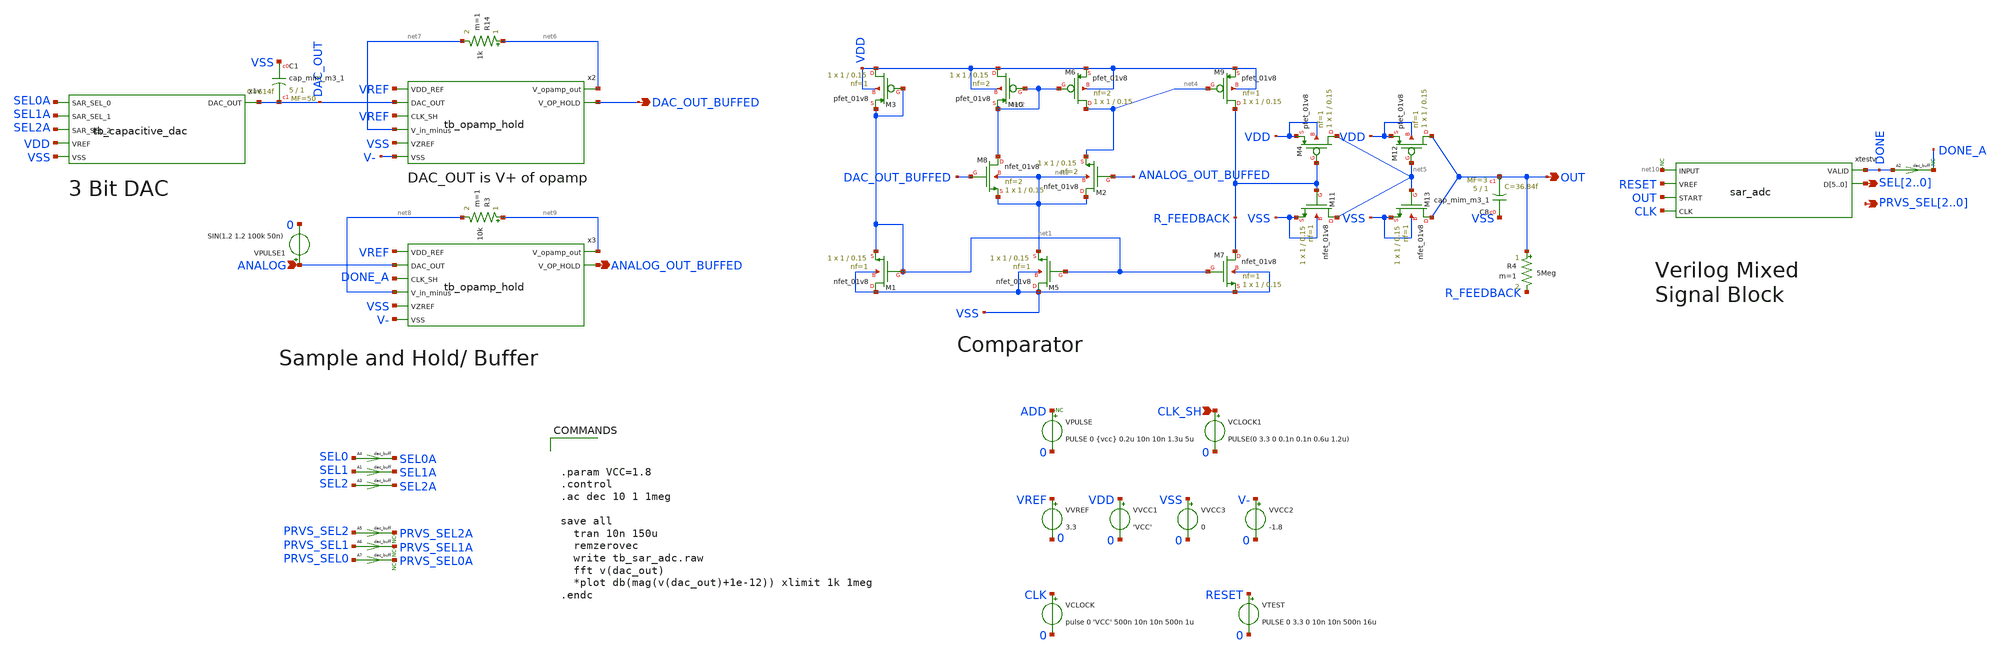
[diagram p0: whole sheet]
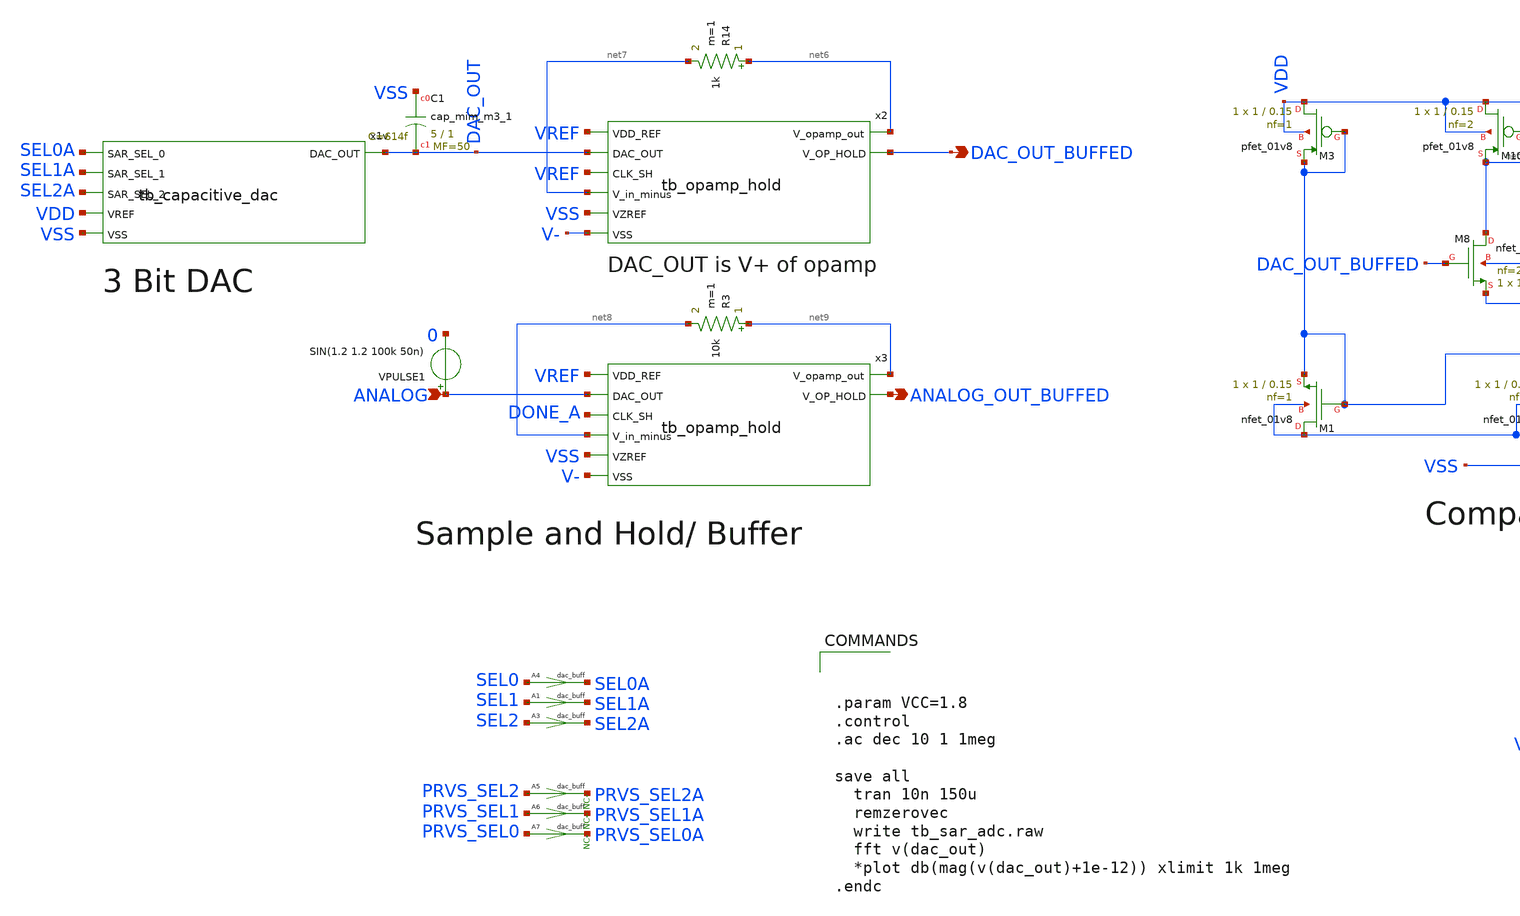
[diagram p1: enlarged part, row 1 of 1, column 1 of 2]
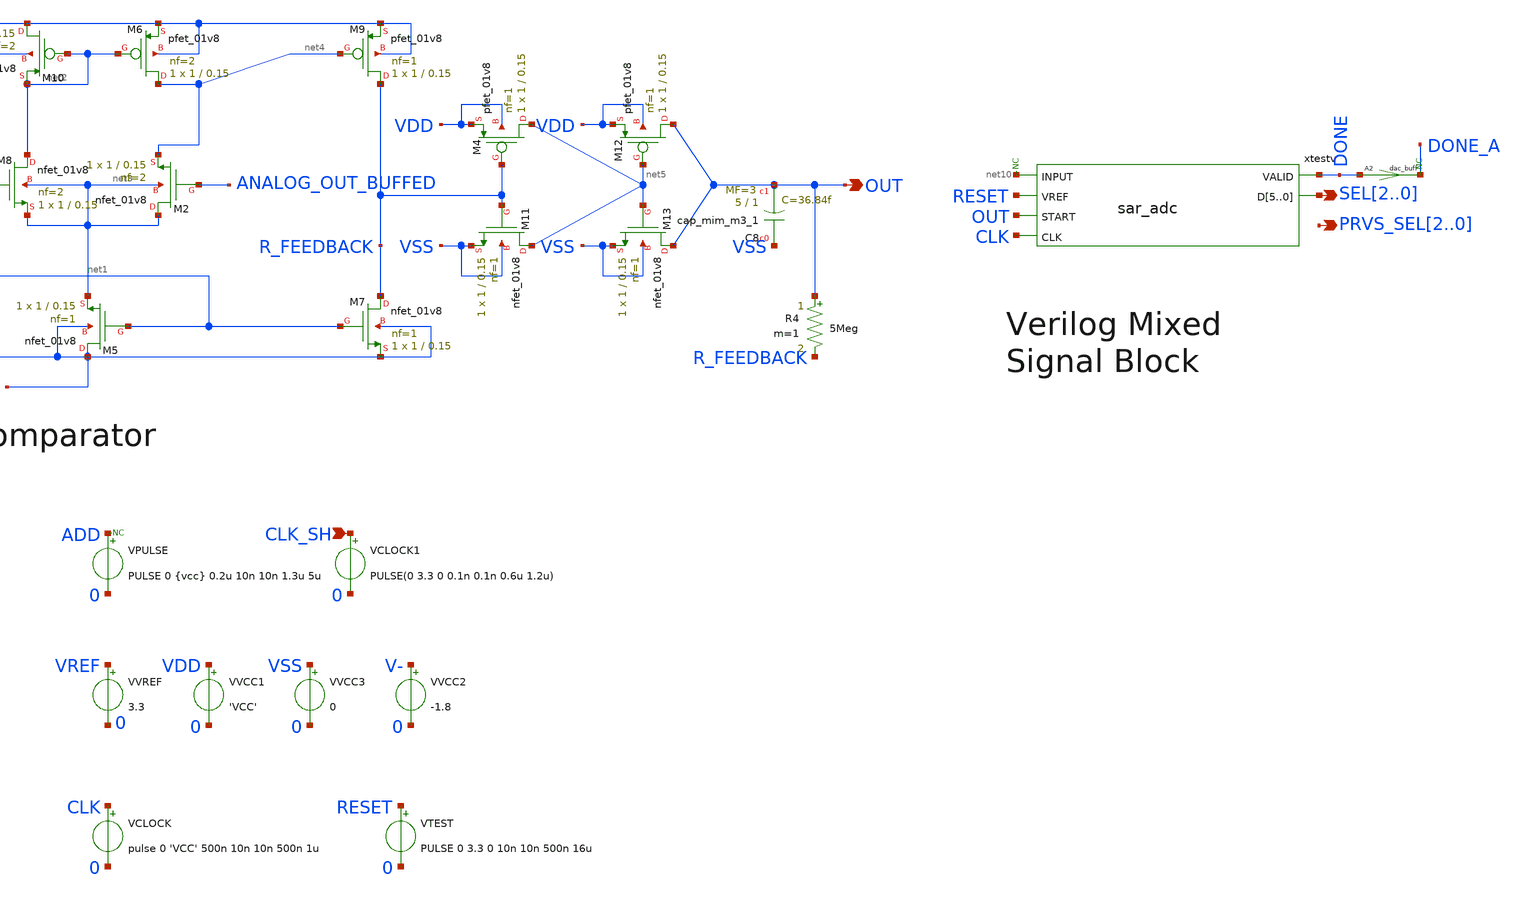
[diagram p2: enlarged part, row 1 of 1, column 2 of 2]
** sch_path: 3bit_sar_adc/tb_sar_adc.sch
**.subckt tb_sar_adc SEL2,SEL1,SEL0 PRVS_SEL2,PRVS_SEL1,PRVS_SEL0 OUT ANALOG DAC_OUT_BUFFED
*+ ANALOG_OUT_BUFFED CLK_SH
*.opin SEL2,SEL1,SEL0
*.opin PRVS_SEL2,PRVS_SEL1,PRVS_SEL0
*.opin OUT
*.ipin ANALOG
*.opin DAC_OUT_BUFFED
*.opin ANALOG_OUT_BUFFED
*.ipin CLK_SH
VPULSE ADD 0 PULSE 0 {vcc} 0.2u 10n 10n 1.3u 5u
VTEST RESET 0 PULSE 0 3.3 0 10n 10n 500n 16u
xtestv net10 RESET OUT DONE SEL2 SEL1 SEL0 SEL2 SEL1 SEL0 CLK sar_adc
A2 [ DONE ] [ DONE_A ] dac_buff
VCLOCK CLK 0 pulse 0 'VCC' 500n 10n 10n 500n 1u
A1 [ SEL1 ] [ SEL1A ] dac_buff
A3 [ SEL2 ] [ SEL2A ] dac_buff
A4 [ SEL0 ] [ SEL0A ] dac_buff
A5 [ PRVS_SEL2 ] [ PRVS_SEL2A ] dac_buff
A6 [ PRVS_SEL1 ] [ PRVS_SEL1A ] dac_buff
A7 [ PRVS_SEL0 ] [ PRVS_SEL0A ] dac_buff
XM9 R_FEEDBACK net4 VDD VDD sky130_fd_pr__pfet_01v8 L=0.15 W=1 nf=1 ad='int((nf+1)/2) * W/nf * 0.29'
+ as='int((nf+2)/2) * W/nf * 0.29' pd='2*int((nf+1)/2) * (W/nf + 0.29)' ps='2*int((nf+2)/2) * (W/nf + 0.29)'
+ nrd='0.29 / W' nrs='0.29 / W' sa=0 sb=0 sd=0 mult=1 m=1
XM6 net4 net2 VDD VDD sky130_fd_pr__pfet_01v8 L=0.15 W=1 nf=2 ad='int((nf+1)/2) * W/nf * 0.29' as='int((nf+2)/2) * W/nf * 0.29'
+ pd='2*int((nf+1)/2) * (W/nf + 0.29)' ps='2*int((nf+2)/2) * (W/nf + 0.29)' nrd='0.29 / W' nrs='0.29 / W'
+ sa=0 sb=0 sd=0 mult=1 m=1
XM10 VDD net2 net2 VDD sky130_fd_pr__pfet_01v8 L=0.15 W=1 nf=2 ad='int((nf+1)/2) * W/nf * 0.29' as='int((nf+2)/2) * W/nf * 0.29'
+ pd='2*int((nf+1)/2) * (W/nf + 0.29)' ps='2*int((nf+2)/2) * (W/nf + 0.29)' nrd='0.29 / W' nrs='0.29 / W'
+ sa=0 sb=0 sd=0 mult=1 m=1
XM3 VDD net1 net1 VDD sky130_fd_pr__pfet_01v8 L=0.15 W=1 nf=1 ad='int((nf+1)/2) * W/nf * 0.29' as='int((nf+2)/2) * W/nf * 0.29'
+ pd='2*int((nf+1)/2) * (W/nf + 0.29)' ps='2*int((nf+2)/2) * (W/nf + 0.29)' nrd='0.29 / W' nrs='0.29 / W'
+ sa=0 sb=0 sd=0 mult=1 m=1
XM4 net5 R_FEEDBACK VDD VDD sky130_fd_pr__pfet_01v8 L=0.15 W=1 nf=1 ad='int((nf+1)/2) * W/nf * 0.29'
+ as='int((nf+2)/2) * W/nf * 0.29' pd='2*int((nf+1)/2) * (W/nf + 0.29)' ps='2*int((nf+2)/2) * (W/nf + 0.29)'
+ nrd='0.29 / W' nrs='0.29 / W' sa=0 sb=0 sd=0 mult=1 m=1
XM12 OUT net5 VDD VDD sky130_fd_pr__pfet_01v8 L=0.15 W=1 nf=1 ad='int((nf+1)/2) * W/nf * 0.29' as='int((nf+2)/2) * W/nf * 0.29'
+ pd='2*int((nf+1)/2) * (W/nf + 0.29)' ps='2*int((nf+2)/2) * (W/nf + 0.29)' nrd='0.29 / W' nrs='0.29 / W'
+ sa=0 sb=0 sd=0 mult=1 m=1
XM2 net3 ANALOG_OUT_BUFFED net4 net3 sky130_fd_pr__nfet_01v8 L=0.15 W=1 nf=2 ad='int((nf+1)/2) * W/nf * 0.29'
+ as='int((nf+2)/2) * W/nf * 0.29' pd='2*int((nf+1)/2) * (W/nf + 0.29)' ps='2*int((nf+2)/2) * (W/nf + 0.29)'
+ nrd='0.29 / W' nrs='0.29 / W' sa=0 sb=0 sd=0 mult=1 m=1
XM1 VSS net1 net1 VSS sky130_fd_pr__nfet_01v8 L=0.15 W=1 nf=1 ad='int((nf+1)/2) * W/nf * 0.29' as='int((nf+2)/2) * W/nf * 0.29'
+ pd='2*int((nf+1)/2) * (W/nf + 0.29)' ps='2*int((nf+2)/2) * (W/nf + 0.29)' nrd='0.29 / W' nrs='0.29 / W'
+ sa=0 sb=0 sd=0 mult=1 m=1
XM5 VSS net1 net3 VSS sky130_fd_pr__nfet_01v8 L=0.15 W=1 nf=1 ad='int((nf+1)/2) * W/nf * 0.29' as='int((nf+2)/2) * W/nf * 0.29'
+ pd='2*int((nf+1)/2) * (W/nf + 0.29)' ps='2*int((nf+2)/2) * (W/nf + 0.29)' nrd='0.29 / W' nrs='0.29 / W'
+ sa=0 sb=0 sd=0 mult=1 m=1
XM7 R_FEEDBACK net1 VSS VSS sky130_fd_pr__nfet_01v8 L=0.15 W=1 nf=1 ad='int((nf+1)/2) * W/nf * 0.29'
+ as='int((nf+2)/2) * W/nf * 0.29' pd='2*int((nf+1)/2) * (W/nf + 0.29)' ps='2*int((nf+2)/2) * (W/nf + 0.29)'
+ nrd='0.29 / W' nrs='0.29 / W' sa=0 sb=0 sd=0 mult=1 m=1
XM8 net2 DAC_OUT_BUFFED net3 net3 sky130_fd_pr__nfet_01v8 L=0.15 W=1 nf=2 ad='int((nf+1)/2) * W/nf * 0.29'
+ as='int((nf+2)/2) * W/nf * 0.29' pd='2*int((nf+1)/2) * (W/nf + 0.29)' ps='2*int((nf+2)/2) * (W/nf + 0.29)'
+ nrd='0.29 / W' nrs='0.29 / W' sa=0 sb=0 sd=0 mult=1 m=1
XM11 net5 R_FEEDBACK VSS VSS sky130_fd_pr__nfet_01v8 L=0.15 W=1 nf=1 ad='int((nf+1)/2) * W/nf * 0.29'
+ as='int((nf+2)/2) * W/nf * 0.29' pd='2*int((nf+1)/2) * (W/nf + 0.29)' ps='2*int((nf+2)/2) * (W/nf + 0.29)'
+ nrd='0.29 / W' nrs='0.29 / W' sa=0 sb=0 sd=0 mult=1 m=1
XM13 OUT net5 VSS VSS sky130_fd_pr__nfet_01v8 L=0.15 W=1 nf=1 ad='int((nf+1)/2) * W/nf * 0.29' as='int((nf+2)/2) * W/nf * 0.29'
+ pd='2*int((nf+1)/2) * (W/nf + 0.29)' ps='2*int((nf+2)/2) * (W/nf + 0.29)' nrd='0.29 / W' nrs='0.29 / W'
+ sa=0 sb=0 sd=0 mult=1 m=1
XC8 VSS OUT sky130_fd_pr__cap_mim_m3_1 W=5 L=1 MF=3 m=3
VVCC1 VDD 0 'VCC'
VPULSE1 ANALOG 0 SIN(1.2 1.2 100k 50n)
x1v DAC_OUT SEL0A SEL1A SEL2A VDD VSS tb_capacitive_dac
x2 VREF DAC_OUT VREF net7 net6 DAC_OUT_BUFFED VSS V- tb_opamp_hold
VVREF VREF 0 3.3
x3 VREF ANALOG DONE_A net8 net9 ANALOG_OUT_BUFFED VSS V- tb_opamp_hold
VVCC3 VSS 0 0
VVCC2 V- 0 -1.8
* noconn DONE_A
* noconn ADD
* noconn PRVS_SEL2A
* noconn PRVS_SEL1A
* noconn PRVS_SEL0A
VCLOCK1 CLK_SH 0 PULSE(0 3.3 0 0.1n 0.1n 0.6u 1.2u)
* noconn #net10
XC1 VSS DAC_OUT sky130_fd_pr__cap_mim_m3_1 W=5 L=1 MF=50 m=50
R14 net6 net7 1k m=1
R3 net9 net8 10k m=1
R4 OUT R_FEEDBACK 5Meg m=1
**** begin user architecture code



.param VCC=1.8
.control
.ac dec 10 1 1meg

save all
  tran 10n 150u
  remzerovec
  write tb_sar_adc.raw
  fft v(dac_out)
  *plot db(mag(v(dac_out)+1e-12)) xlimit 1k 1meg
.endc



** opencircuitdesign pdks install
.lib $::SKYWATER_MODELS/sky130.lib.spice tt
.include $::SKYWATER_STDCELLS/sky130_fd_sc_hd.spice
.include /foss/pdks/sky130A/libs.tech/xschem/sky130_stdcells/

**** end user architecture code
**.ends

* expanding   symbol:  /foss/designs/3bit_sar_adc/3bit_sar_adc/sar_adc.sym # of pins=6
** sym_path: /foss/designs/3bit_sar_adc/3bit_sar_adc/sar_adc.sym
** sch_path: /foss/designs/3bit_sar_adc/3bit_sar_adc/sar_adc.sch
.subckt sar_adc INPUT VREF START VALID D5 D4 D3 D2 D1 D0 CLK
*.ipin INPUT
*.ipin VREF
*.ipin START
*.opin VALID
*.ipin CLK
*.opin D5,D4,D3,D2,D1,D0
CLAST TEST_V 0 '1p / 32' m=1
ACOMP [ %vd(TEST_V VREF) ] [ COMP ] comparator
XSAMPLE INPUT IIN SAMPLE VREF tgate
R1 IIN TEST_V 1k m=1
ADUT [ CLK COMP START ] [ SAMPLE ~D5 ~D4 ~D3 VALID VALID VALID ] dut
A1 [ COMP ] [ COMP_A ] dac_buff
* noconn D[5..0]
* noconn COMP
* noconn %vd(TEST_V VREF)
xb6 TEST_V VREF D5 ccap C=1p,'1p/2','1p/4','1p/8','1p/16','1p/32'
xb5 TEST_V VREF D4 ccap C=1p,'1p/2','1p/4','1p/8','1p/16','1p/32'
xb4 TEST_V VREF D3 ccap C=1p,'1p/2','1p/4','1p/8','1p/16','1p/32'
xb3 TEST_V VREF D2 ccap C=1p,'1p/2','1p/4','1p/8','1p/16','1p/32'
xb2 TEST_V VREF D1 ccap C=1p,'1p/2','1p/4','1p/8','1p/16','1p/32'
xb1 TEST_V VREF D0 ccap C=1p,'1p/2','1p/4','1p/8','1p/16','1p/32'
.ends


* expanding   symbol:  /foss/designs/3bit_sar_adc/3bit_sar_adc/tb_capacitive_dac.sym # of pins=6
** sym_path: /foss/designs/3bit_sar_adc/3bit_sar_adc/tb_capacitive_dac.sym
** sch_path: /foss/designs/3bit_sar_adc/3bit_sar_adc/tb_capacitive_dac.sch
.subckt tb_capacitive_dac DAC_OUT SAR_SEL_0 SAR_SEL_1 SAR_SEL_2 VREF VSS
*.opin DAC_OUT
*.ipin SAR_SEL_1
*.ipin SAR_SEL_0
*.ipin SAR_SEL_2
*.ipin VREF
*.ipin VSS
XM20 VSS SAR_SEL_2 S2 S2 sky130_fd_pr__pfet_01v8 L=0.15 W=100 nf=4 ad='int((nf+1)/2) * W/nf * 0.29' as='int((nf+2)/2) * W/nf * 0.29'
+ pd='2*int((nf+1)/2) * (W/nf + 0.29)' ps='2*int((nf+2)/2) * (W/nf + 0.29)' nrd='0.29 / W' nrs='0.29 / W'
+ sa=0 sb=0 sd=0 mult=1 m=1
XM21 VREF SAR_SEL_2 S2 S2 sky130_fd_pr__nfet_01v8 L=0.15 W=150 nf=4 ad='int((nf+1)/2) * W/nf * 0.29'
+ as='int((nf+2)/2) * W/nf * 0.29' pd='2*int((nf+1)/2) * (W/nf + 0.29)' ps='2*int((nf+2)/2) * (W/nf + 0.29)'
+ nrd='0.29 / W' nrs='0.29 / W' sa=0 sb=0 sd=0 mult=1 m=1
XC16 net1 S1 sky130_fd_pr__cap_mim_m3_1 W=5 L=1 MF=400 m=400
XC18 net1 S0 sky130_fd_pr__cap_mim_m3_1 W=5 L=1 MF=200 m=200
XM22 VSS SAR_SEL_1 S1 S1 sky130_fd_pr__pfet_01v8 L=0.15 W=100 nf=10 ad='int((nf+1)/2) * W/nf * 0.29'
+ as='int((nf+2)/2) * W/nf * 0.29' pd='2*int((nf+1)/2) * (W/nf + 0.29)' ps='2*int((nf+2)/2) * (W/nf + 0.29)'
+ nrd='0.29 / W' nrs='0.29 / W' sa=0 sb=0 sd=0 mult=1 m=1
XM23 VREF SAR_SEL_1 S1 S1 sky130_fd_pr__nfet_01v8 L=0.15 W=150 nf=4 ad='int((nf+1)/2) * W/nf * 0.29'
+ as='int((nf+2)/2) * W/nf * 0.29' pd='2*int((nf+1)/2) * (W/nf + 0.29)' ps='2*int((nf+2)/2) * (W/nf + 0.29)'
+ nrd='0.29 / W' nrs='0.29 / W' sa=0 sb=0 sd=0 mult=1 m=1
XM24 VSS SAR_SEL_0 S0 S0 sky130_fd_pr__pfet_01v8 L=0.15 W=100 nf=4 ad='int((nf+1)/2) * W/nf * 0.29' as='int((nf+2)/2) * W/nf * 0.29'
+ pd='2*int((nf+1)/2) * (W/nf + 0.29)' ps='2*int((nf+2)/2) * (W/nf + 0.29)' nrd='0.29 / W' nrs='0.29 / W'
+ sa=0 sb=0 sd=0 mult=1 m=1
XM25 VREF SAR_SEL_0 S0 S0 sky130_fd_pr__nfet_01v8 L=0.15 W=150 nf=4 ad='int((nf+1)/2) * W/nf * 0.29'
+ as='int((nf+2)/2) * W/nf * 0.29' pd='2*int((nf+1)/2) * (W/nf + 0.29)' ps='2*int((nf+2)/2) * (W/nf + 0.29)'
+ nrd='0.29 / W' nrs='0.29 / W' sa=0 sb=0 sd=0 mult=1 m=1
XC22 DAC_OUT VSS sky130_fd_pr__cap_mim_m3_1 W=5 L=1 MF=20 m=20
XC2 net1 S2 sky130_fd_pr__cap_mim_m3_1 W=5 L=1 MF=825 m=825
XC6 VSS S2 sky130_fd_pr__cap_mim_m3_1 W=5 L=1 MF=200 m=200
XC5 VSS S1 sky130_fd_pr__cap_mim_m3_1 W=5 L=1 MF=200 m=200
XC7 VSS S0 sky130_fd_pr__cap_mim_m3_1 W=5 L=1 MF=100 m=100
**** begin user architecture code




.param CAP=80



**** end user architecture code
R1 net1 DAC_OUT 10 m=1
.ends


* expanding   symbol:  /foss/designs/3bit_sar_adc/3bit_sar_adc/tb_opamp_hold.sym # of pins=8
** sym_path: /foss/designs/3bit_sar_adc/3bit_sar_adc/tb_opamp_hold.sym
** sch_path: /foss/designs/3bit_sar_adc/3bit_sar_adc/tb_opamp_hold.sch
.subckt tb_opamp_hold VDD_REF DAC_OUT CLK_SH V_in_minus V_opamp_out V_OP_HOLD VZREF VSS
*.opin V_opamp_out
*.ipin DAC_OUT
*.ipin CLK_SH
*.opin V_OP_HOLD
*.ipin VDD_REF
*.ipin VZREF
*.ipin VSS
*.ipin V_in_minus
XM82 net1 V_in_minus net3 net3 sky130_fd_pr__pfet_01v8 L=0.6 W=6 nf=1 ad='W * 0.29' as='W * 0.29' pd='2 * (W + 0.29)'
+ ps='2 * (W + 0.29)' nrd='0.29 / W' nrs='0.29 / W' sa=0 sb=0 sd=0 mult=1 m=1
XM84 net2 DAC_OUT net3 net3 sky130_fd_pr__pfet_01v8 L=0.6 W=6 nf=1 ad='W * 0.29' as='W * 0.29' pd='2 * (W + 0.29)'
+ ps='2 * (W + 0.29)' nrd='0.29 / W' nrs='0.29 / W' sa=0 sb=0 sd=0 mult=1 m=1
XM85 net1 net1 VSS VSS sky130_fd_pr__nfet_01v8 L=0.6 W=6 nf=1 ad='W * 0.29' as='W * 0.29' pd='2 * (W + 0.29)'
+ ps='2 * (W + 0.29)' nrd='0.29 / W' nrs='0.29 / W' sa=0 sb=0 sd=0 mult=1 m=1
XM86 net2 net1 VSS VSS sky130_fd_pr__nfet_01v8 L=0.6 W=6 nf=1 ad='W * 0.29' as='W * 0.29' pd='2 * (W + 0.29)'
+ ps='2 * (W + 0.29)' nrd='0.29 / W' nrs='0.29 / W' sa=0 sb=0 sd=0 mult=1 m=1
XM87 net3 VSS VDD_REF VDD_REF sky130_fd_pr__pfet_01v8 L=0.6 W=6 nf=1 ad='W * 0.29' as='W * 0.29' pd='2 * (W + 0.29)'
+ ps='2 * (W + 0.29)' nrd='0.29 / W' nrs='0.29 / W' sa=0 sb=0 sd=0 mult=1 m=1
XM88 V_opamp_out VSS VDD_REF VDD_REF sky130_fd_pr__pfet_01v8 L=0.6 W=6 nf=1 ad='W * 0.29' as='W * 0.29'
+ pd='2 * (W + 0.29)' ps='2 * (W + 0.29)' nrd='0.29 / W' nrs='0.29 / W' sa=0 sb=0 sd=0 mult=1 m=1
XM89 VZREF VSS VDD_REF VDD_REF sky130_fd_pr__pfet_01v8 L=0.6 W=6 nf=1 ad='W * 0.29' as='W * 0.29' pd='2 * (W + 0.29)'
+ ps='2 * (W + 0.29)' nrd='0.29 / W' nrs='0.29 / W' sa=0 sb=0 sd=0 mult=1 m=1
XM90 net4 VDD_REF net2 VSS sky130_fd_pr__nfet_01v8 L=0.6 W=1 nf=1 ad='W * 0.29' as='W * 0.29' pd='2 * (W + 0.29)'
+ ps='2 * (W + 0.29)' nrd='0.29 / W' nrs='0.29 / W' sa=0 sb=0 sd=0 mult=1 m=1
XM91 V_opamp_out net2 VSS VSS sky130_fd_pr__nfet_01v8 L=0.6 W=6 nf=1 ad='W * 0.29' as='W * 0.29' pd='2 * (W + 0.29)'
+ ps='2 * (W + 0.29)' nrd='0.29 / W' nrs='0.29 / W' sa=0 sb=0 sd=0 mult=1 m=1
XR10 VSS VZREF VSS sky130_fd_pr__res_high_po W=1 L=1 mult=1 m=1
XR13 VZREF VDD_REF VSS sky130_fd_pr__res_high_po W=1 L=1 mult=1 m=1
C34 V_opamp_out net4 0.8p m=1
XM80 V_OP_HOLD CLK_SH V_opamp_out VZREF sky130_fd_pr__nfet_01v8 L=0.6 W=6 nf=1 ad='W * 0.29' as='W * 0.29'
+ pd='2 * (W + 0.29)' ps='2 * (W + 0.29)' nrd='0.29 / W' nrs='0.29 / W' sa=0 sb=0 sd=0 mult=1 m=1
XC1 V_OP_HOLD VZREF sky130_fd_pr__cap_mim_m3_1 W=5 L=1 MF=42 m=42
.ends


* expanding   symbol:  tgate.sym # of pins=4
** sym_path: tgate.sym
** sch_path: tgate.sch
.subckt tgate A B CTL VDD
*.ipin CTL
*.iopin B
*.iopin A
*.ipin VDD
SWITCH A B CTL 0 TG
* noconn VDD
.ends


* expanding   symbol:  ccap.sym # of pins=3
** sym_path: ccap.sym
** sch_path: ccap.sch
.subckt ccap IN VCC CTL  C=1p
*.ipin IN
*.ipin VCC
*.ipin CTL
XINV CTL TAIL VCC ainv
CB IN TAIL c='C' m=1
.ends


* expanding   symbol:  ainv.sym # of pins=3
** sym_path: ainv.sym
** sch_path: ainv.sch
.subckt ainv IN OUT VDD
*.ipin IN
*.opin OUT
*.ipin VDD
MN OUT IN 0 0 N1
MP OUT IN VDD VDD P1
.ends

**** begin user architecture code
.model dut d_cosim simulation="ivlng" sim_args=["adc"]
.model comparator adc_bridge in_low=0 in_high=0
.model n1 nmos   level=2 vto=0.5 kp=24e-6 gamma=0.15 phi=0.65 lambda=0.015 xj=0.5e-6

.model p1 pmos   level=2 vto=-0.5 kp=8.5e-6 gamma=0.4 phi=0.65 lambda=0.05 xj=0.5e-6

.MODEL TG SW( VT=1.5 RON=2k )
.model dac_buff dac_bridge input_load=1e-15 t_rise=10n t_fall=10n  out_low=0 out_high=3.3
**** end user architecture code
.end
